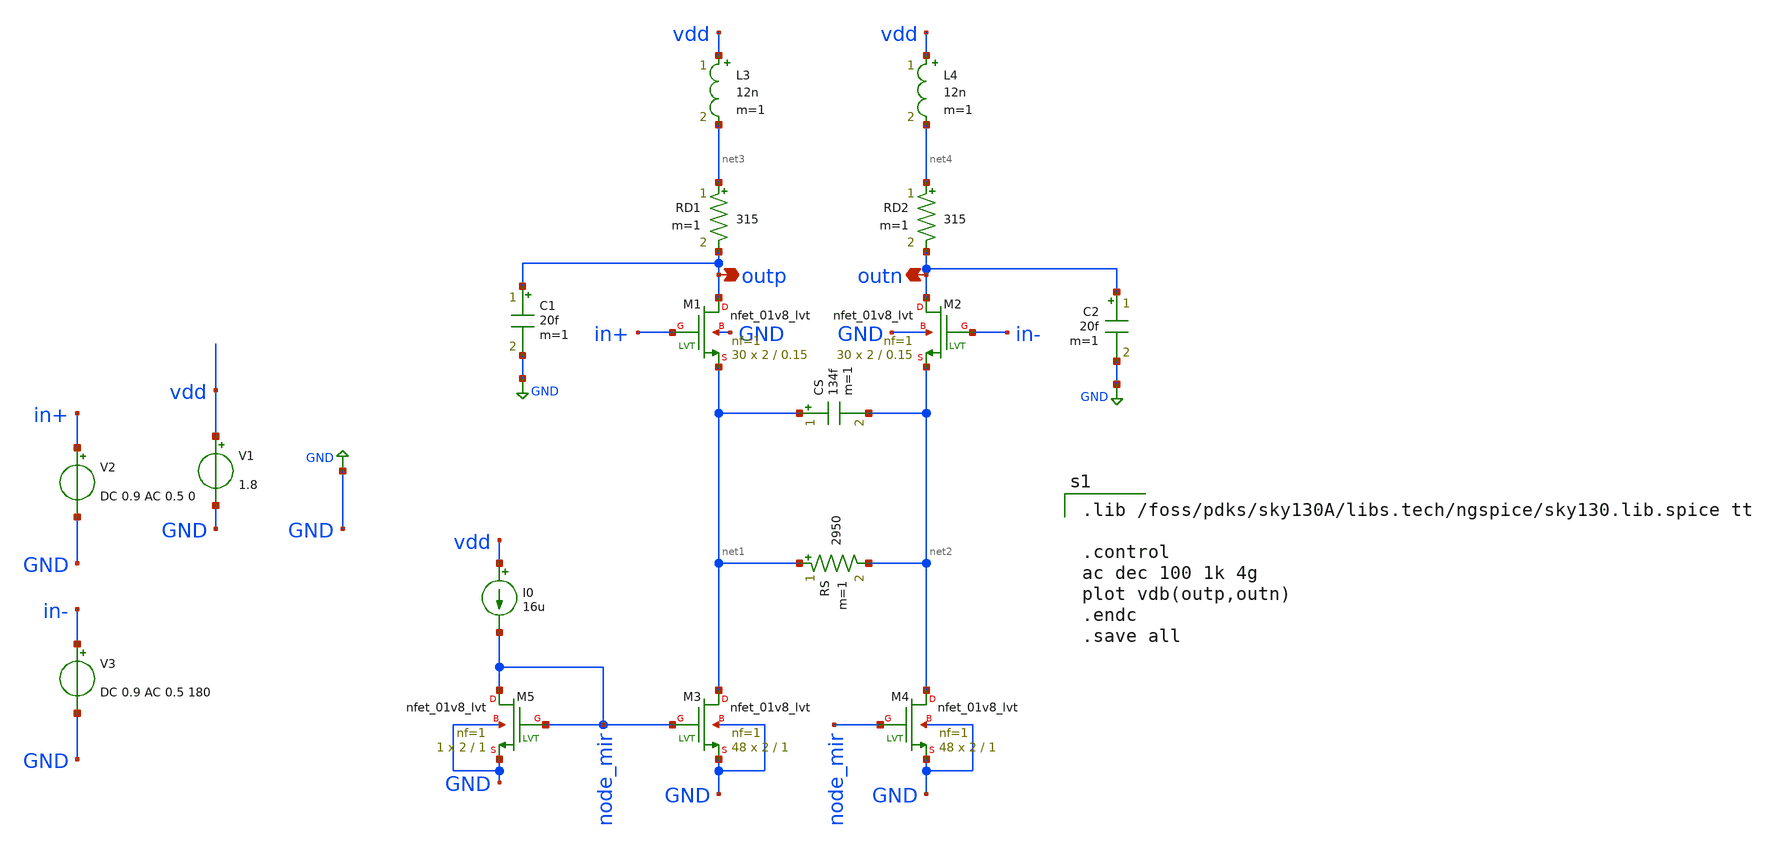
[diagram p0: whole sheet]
** sch_path: CTLE/ctle_20db.sch
**.subckt ctle_20db outp outn
*.opin outp
*.opin outn
V1 vdd GND 1.8
V2 in+ GND DC 0.9 AC 0.5 0
V3 in- GND DC 0.9 AC 0.5 180
XM1 outp in+ net1 GND sky130_fd_pr__nfet_01v8_lvt L=0.15 W=2 nf=1 ad='int((nf+1)/2) * W/nf * 0.29' as='int((nf+2)/2) * W/nf * 0.29'
+ pd='2*int((nf+1)/2) * (W/nf + 0.29)' ps='2*int((nf+2)/2) * (W/nf + 0.29)' nrd='0.29 / W' nrs='0.29 / W'
+ sa=0 sb=0 sd=0 mult=30 m=30
XM2 outn in- net2 GND sky130_fd_pr__nfet_01v8_lvt L=0.15 W=2 nf=1 ad='int((nf+1)/2) * W/nf * 0.29' as='int((nf+2)/2) * W/nf * 0.29'
+ pd='2*int((nf+1)/2) * (W/nf + 0.29)' ps='2*int((nf+2)/2) * (W/nf + 0.29)' nrd='0.29 / W' nrs='0.29 / W'
+ sa=0 sb=0 sd=0 mult=30 m=30
I0 vdd node_mir 16u
XM3 net1 node_mir GND GND sky130_fd_pr__nfet_01v8_lvt L=1 W=2 nf=1 ad='int((nf+1)/2) * W/nf * 0.29' as='int((nf+2)/2) * W/nf * 0.29'
+ pd='2*int((nf+1)/2) * (W/nf + 0.29)' ps='2*int((nf+2)/2) * (W/nf + 0.29)' nrd='0.29 / W' nrs='0.29 / W'
+ sa=0 sb=0 sd=0 mult=48 m=48
XM4 net2 node_mir GND GND sky130_fd_pr__nfet_01v8_lvt L=1 W=2 nf=1 ad='int((nf+1)/2) * W/nf * 0.29' as='int((nf+2)/2) * W/nf * 0.29'
+ pd='2*int((nf+1)/2) * (W/nf + 0.29)' ps='2*int((nf+2)/2) * (W/nf + 0.29)' nrd='0.29 / W' nrs='0.29 / W'
+ sa=0 sb=0 sd=0 mult=48 m=48
XM5 node_mir node_mir GND GND sky130_fd_pr__nfet_01v8_lvt L=1 W=2 nf=1 ad='int((nf+1)/2) * W/nf * 0.29'
+ as='int((nf+2)/2) * W/nf * 0.29' pd='2*int((nf+1)/2) * (W/nf + 0.29)' ps='2*int((nf+2)/2) * (W/nf + 0.29)'
+ nrd='0.29 / W' nrs='0.29 / W' sa=0 sb=0 sd=0 mult=1 m=1
RD1 net3 outp 315 m=1
RD2 net4 outn 315 m=1
CS net1 net2 134f m=1
RS net1 net2 2950 m=1
L3 vdd net3 12n m=1
L4 vdd net4 12n m=1
C1 outp GND 20f m=1
C2 outn GND 20f m=1
**** begin user architecture code

.lib /foss/pdks/sky130A/libs.tech/ngspice/sky130.lib.spice tt

.control
ac dec 100 1k 4g
plot vdb(outp,outn)
.endc
.save all


**** end user architecture code
**.ends
.GLOBAL GND
.end
